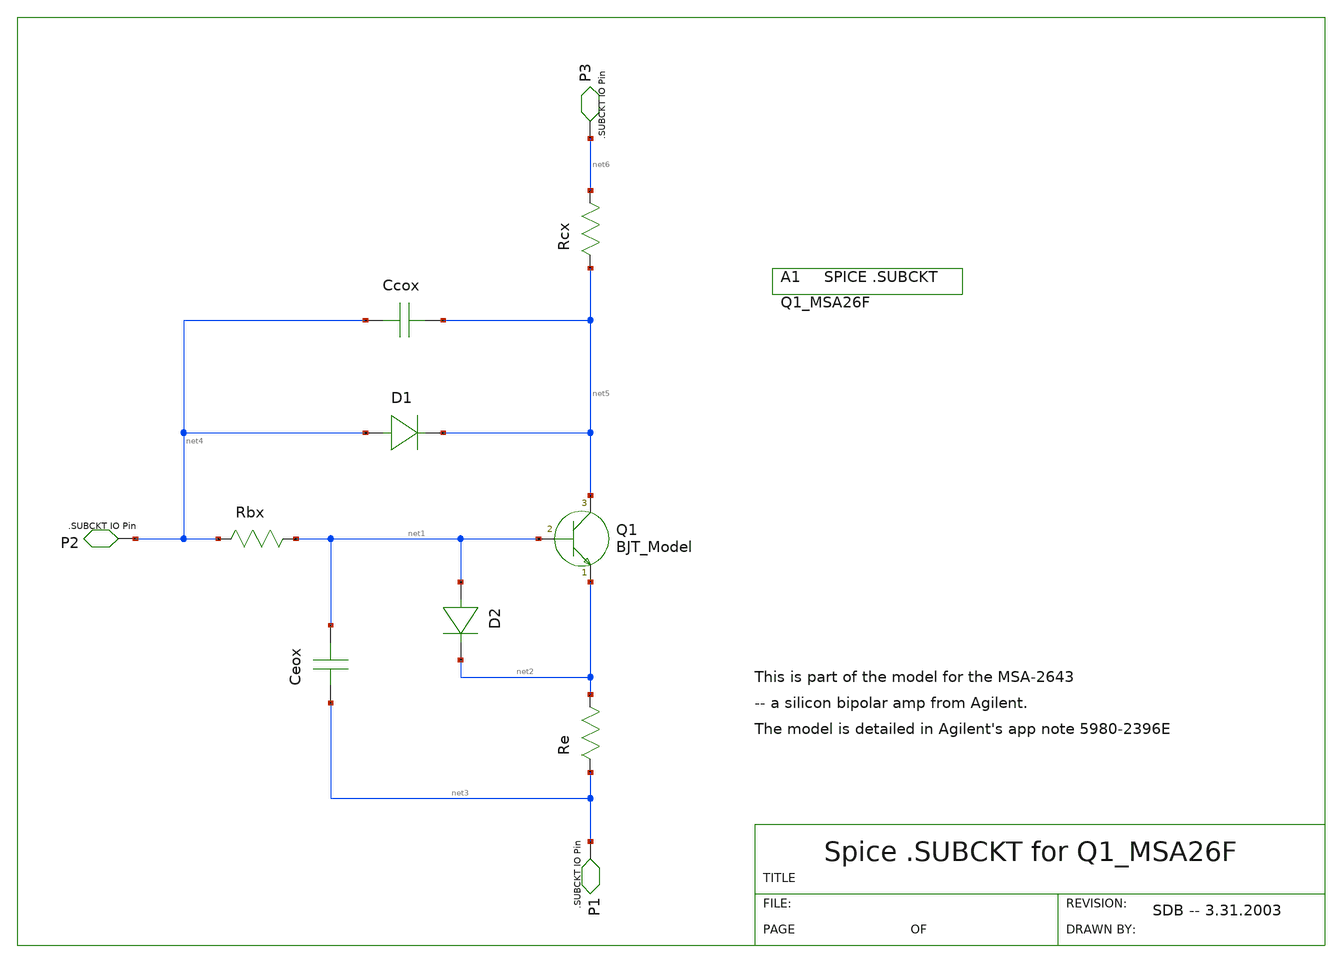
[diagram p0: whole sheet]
** sch_path: xschem_library/gschem_import/Q1.sch
**.subckt Q1
Q1 net5 net1 net2
D1 net4 net5
D2 net1 net2
Ccox net4 net5 1.851e-14F
Ceox net3 net1 6.01e-15F
Rbx net1 net4 3.723
Rcx net6 net5 6.386
Re net2 net3 2.158
P3 net6
P2 net4
P1 net3
A1
**.ends
.end
